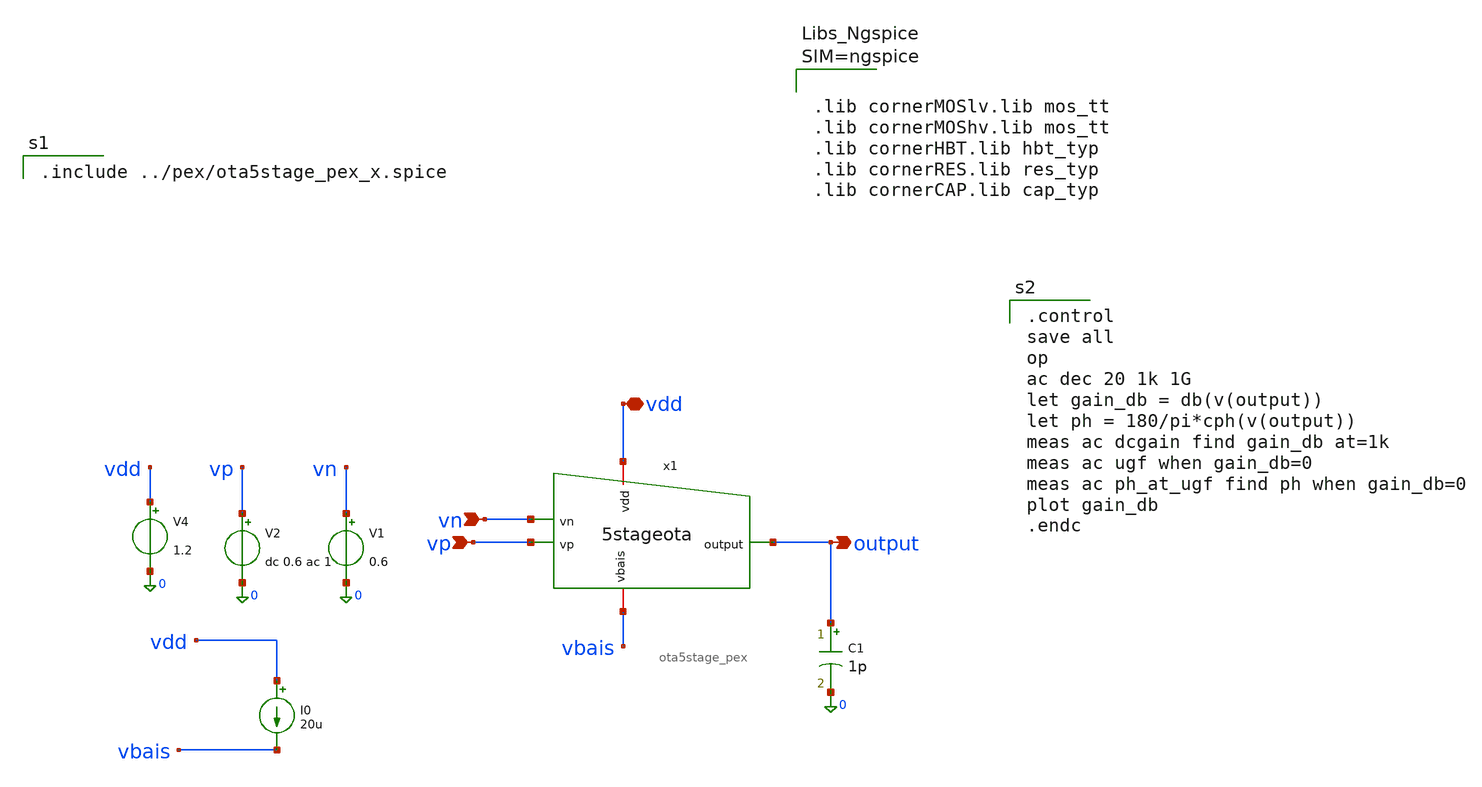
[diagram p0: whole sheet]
** sch_path: xschem/TB5OTA_pex.sch
**.subckt TB5OTA_pex vp vdd output vn
*.ipin vp
*.iopin vdd
*.opin output
*.ipin vn
C1 output 0 1p m=1
V1 vn 0 0.6
V2 vp 0 dc 0.6 ac 1
V4 vdd 0 1.2
I0 vdd vbais 20u
x1 vbais vdd output vn vp ota5stage_pex
**** begin user architecture code



.lib cornerMOSlv.lib mos_tt
.lib cornerMOShv.lib mos_tt
.lib cornerHBT.lib hbt_typ
.lib cornerRES.lib res_typ
.lib cornerCAP.lib cap_typ




.include ../pex/ota5stage_pex_x.spice


.control
save all
op
ac dec 20 1k 1G
let gain_db = db(v(output))
let ph = 180/pi*cph(v(output))
meas ac dcgain find gain_db at=1k
meas ac ugf when gain_db=0
meas ac ph_at_ugf find ph when gain_db=0
plot gain_db
.endc

**** end user architecture code
**.ends
.end
